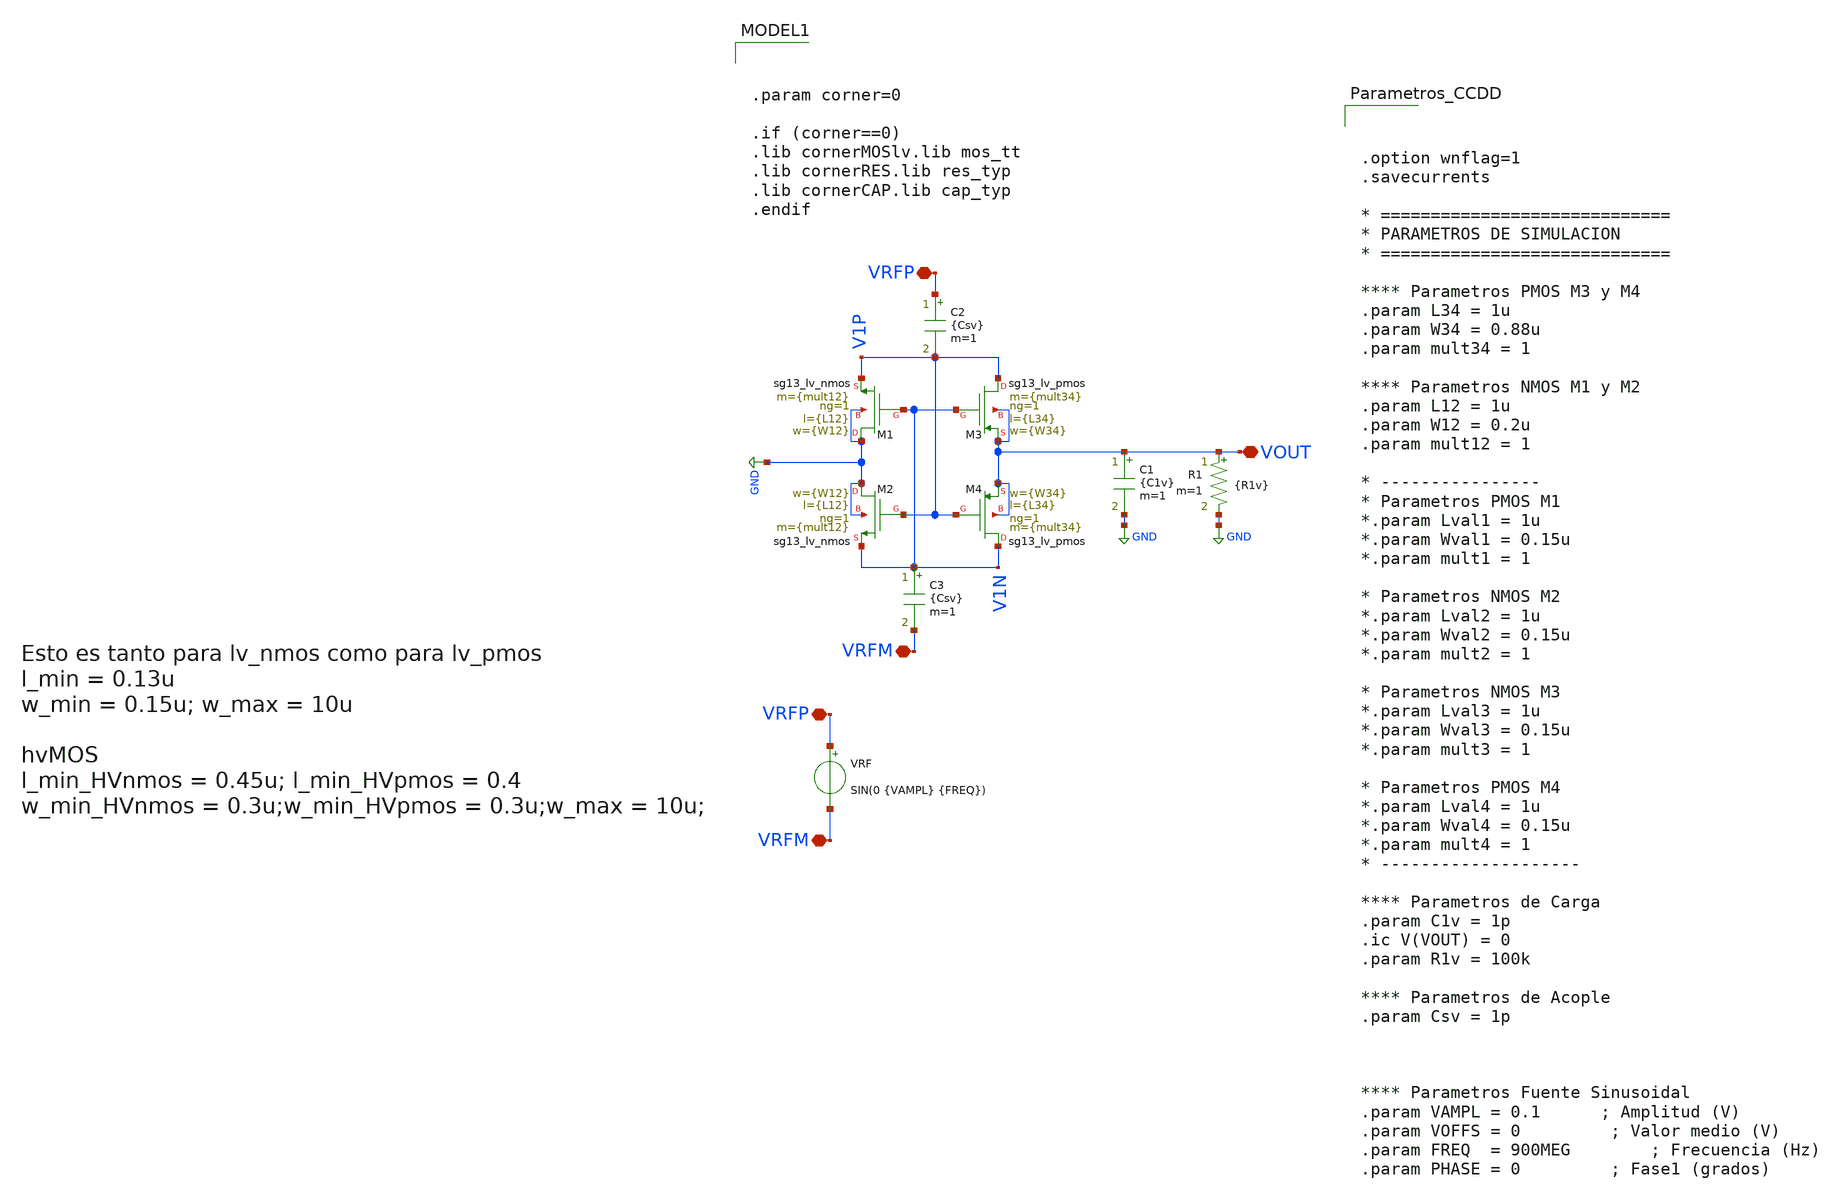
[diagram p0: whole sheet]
** sch_path: Esquematicos_Xschem/Memoria_CCDD_TRAN.sch
**.subckt Memoria_CCDD_TRAN VRFP VRFM VOUT VRFP VRFM
*.iopin VRFP
*.iopin VRFM
*.iopin VOUT
*.iopin VRFP
*.iopin VRFM
XM3 V1P V1N VOUT VOUT sg13_lv_pmos w={W34} l={L34} ng=1 m={mult34} mm_ok=1
XM2 GND V1P V1N GND sg13_lv_nmos w={W12} l={L12} ng=1 m={mult12} mm_ok=1
XM1 GND V1N V1P GND sg13_lv_nmos w={W12} l={L12} ng=1 m={mult12} mm_ok=1
XM4 V1N V1P VOUT VOUT sg13_lv_pmos w={W34} l={L34} ng=1 m={mult34} mm_ok=1
R1 VOUT GND {R1v} m=1
C1 VOUT GND {C1v} m=1
VRF VRFP VRFM SIN(0 {VAMPL} {FREQ})
.save i(vrf)
C2 VRFP V1P {Csv} m=1
C3 V1N VRFM {Csv} m=1
**** begin user architecture code


.param corner=0

.if (corner==0)
.lib cornerMOSlv.lib mos_tt
.lib cornerRES.lib res_typ
.lib cornerCAP.lib cap_typ
.endif




.option wnflag=1
.savecurrents

* =============================
* PARAMETROS DE SIMULACION
* =============================

**** Parametros PMOS M3 y M4
.param L34 = 1u
.param W34 = 0.88u
.param mult34 = 1

**** Parametros NMOS M1 y M2
.param L12 = 1u
.param W12 = 0.2u
.param mult12 = 1

* ----------------
* Parametros PMOS M1
*.param Lval1 = 1u
*.param Wval1 = 0.15u
*.param mult1 = 1

* Parametros NMOS M2
*.param Lval2 = 1u
*.param Wval2 = 0.15u
*.param mult2 = 1

* Parametros NMOS M3
*.param Lval3 = 1u
*.param Wval3 = 0.15u
*.param mult3 = 1

* Parametros PMOS M4
*.param Lval4 = 1u
*.param Wval4 = 0.15u
*.param mult4 = 1
* --------------------

**** Parametros de Carga
.param C1v = 1p
.ic V(VOUT) = 0
.param R1v = 100k

**** Parametros de Acople
.param Csv = 1p



**** Parametros Fuente Sinusoidal
.param VAMPL = 0.1      ; Amplitud (V)
.param VOFFS = 0         ; Valor medio (V)
.param FREQ  = 900MEG        ; Frecuencia (Hz)
.param PHASE = 0         ; Fase1 (grados)








.option wnflag=1
.savecurrents

* ==============================================
* BLOQUE DE CONTROL NGSPICE
* ==============================================
.control

**** Compatibilidad y Color
  set filetype = ascii
  set color0 = white

**** Inicializacion de Parametro While
  let k = 0
  let start_VRF = 0.3
  let stop_VRF = 1.2
  let delta_VRF = 0.1
  let VRF_act = start_VRF

**** Inicializacion Constantes para Calculos
  let i = 0
  let IDmax = 0
  let IGmax = 0
  let VDSmax = 0
  let VGSmax = 0

**** Variables Extriores


* ==============================================
* Inicio del While
* ==============================================
  while VRF_act le stop_VRF + 2*delta_VRF
    if k = 1
      tran 20p 500n UIC
    end
    alterparam VAMPL = $&VRF_act
    reset


* -----------------------------
* Almacenamiento de Variables
* -----------------------------
    save all

    **** M1
    save @n.xm1.nsg13_lv_nmos[ids]
    save @n.xm1.nsg13_lv_nmos[gm]
    save @n.xm1.nsg13_lv_nmos[gds]
    save @n.xm1.nsg13_lv_nmos[vth]

    **** M2
    save @n.xm2.nsg13_lv_nmos[ids]
    save @n.xm2.nsg13_lv_nmos[gm]
    save @n.xm2.nsg13_lv_nmos[gds]
    save @n.xm2.nsg13_lv_nmos[vth]

    **** M3
    save @n.xm3.nsg13_lv_pmos[ids]
    save @n.xm3.nsg13_lv_pmos[gm]
    save @n.xm3.nsg13_lv_pmos[gds]
    save @n.xm3.nsg13_lv_pmos[vth]

    **** M4
    save @n.xm4.nsg13_lv_pmos[ids]
    save @n.xm4.nsg13_lv_pmos[gm]
    save @n.xm4.nsg13_lv_pmos[gds]
    save @n.xm4.nsg13_lv_pmos[vth]

    **** Fuente de Voltaje
    save @VRF[i]
    save @VRF[p]

    **** Carga
    save R1[i]
    save C1[i]


* ----------------------------------------------
* Definicion de Varriables Internas
* ----------------------------------------------
    if k = 1

      **** M1
      let ids1 = @n.xm1.nsg13_lv_nmos[ids]
      let gm1 = @n.xm1.nsg13_lv_nmos[gm]
      let gds1 = @n.xm1.nsg13_lv_nmos[gds]
      let vth1 = @n.xm1.nsg13_lv_nmos[vth]
      let VDS1 = V1P - 0
      let VGS1 = V1N - 0

      **** M2
      let ids2 = @n.xm2.nsg13_lv_nmos[ids]
      let gm2 = @n.xm2.nsg13_lv_nmos[gm]
      let gds2 =  @n.xm2.nsg13_lv_nmos[gds]
      let vth2 = @n.xm2.nsg13_lv_nmos[vth]
      let VDS2 = V1N - 0
      let VGS2 = V1P - 0

      **** M3
      let ids3 = @n.xm3.nsg13_lv_pmos[ids]
      let gm3 = @n.xm3.nsg13_lv_pmos[gm]
      let gds3 = @n.xm3.nsg13_lv_pmos[gds]
      let vth3 = @n.xm3.nsg13_lv_pmos[vth]
      let VSD3 = VOUT - V1P
      let VSG3 = VOUT - V1N

      **** M4
      let ids4 = @n.xm4.nsg13_lv_pmos[ids]
      let gm4 = @n.xm4.nsg13_lv_pmos[gm]
      let gds4 = @n.xm4.nsg13_lv_pmos[gds]
      let vth4 = @n.xm4.nsg13_lv_pmos[vth]
      let VSD4 = VOUT - V1N
      let VSG4 = VOUT - V1P

      **** Fuente de Voltaje
      let IRF = @VRF[i]
      let PRF = @VRF[p]
      let VRF = VRFP - VRFM

      **** Carga
      let IC = @C1[i]
      let IR = @R1[i]
      let IRC = IC + IR
      let PR = IR * VOUT

    end


* ==============================================
* RESULTADOS
* ==============================================

* -----------------------------
* Graficas de la Simulacion
* -----------------------------
    **** Fuente
    *plot VRF vs time
    *plot IRF vs time

    **** Carga
    plot VOUT VRF vs time
    *plot IRC vs time
    *plot avg(PR/PRF)

* -----------------------------
* Registro de Datos
* -----------------------------
    remzerovec
    write Memoria_CCDD2_TRAN_MULT1_L01-00_W00-20_R100k_M1_C01-00.csv time VRF IRF VOUT IC IR VDS1
+ VDS2 VSD3 VSD4 VGS1 VGS2 VSG3 VSG4 ids1 ids2 ids3 ids4 igs1 igs2 igs3 igs4 vth1 vth2 vth3 vth4


* ==============================================
* CIERRE DE WHILE
* ==============================================
    **** Definicion de proximo valor (while)
    let VRF_act = VRF_act + delta_VRF
    let k = 1
    set appendwrite

  end

.endc


**** end user architecture code
**.ends
.GLOBAL GND
.end
